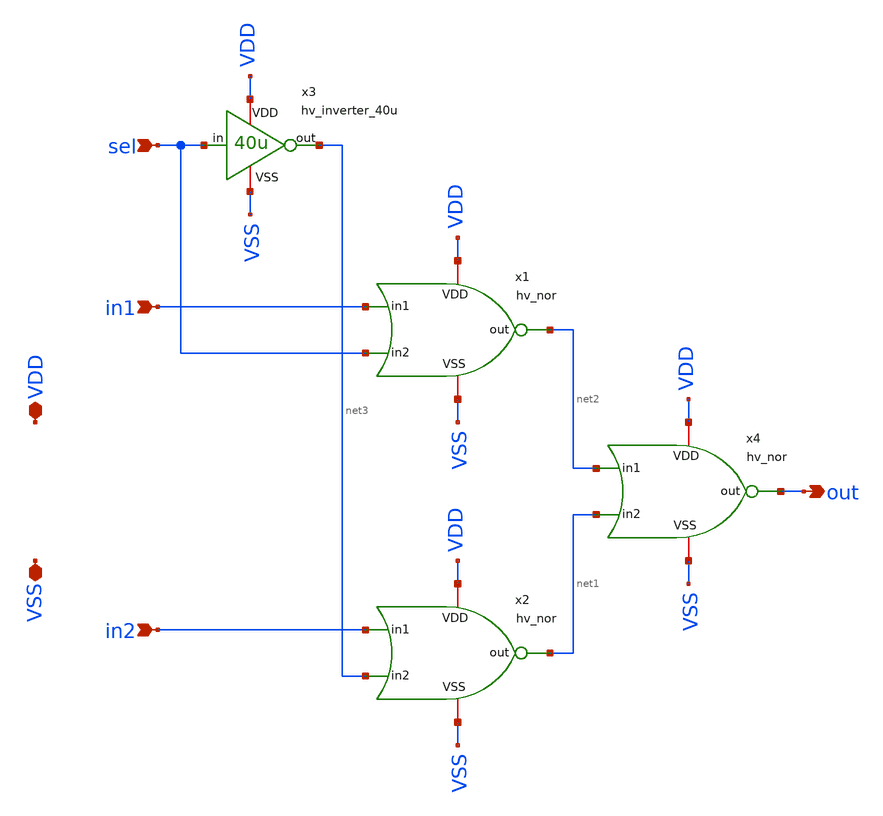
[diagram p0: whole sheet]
** sch_path: macros/heichips26_vcr/macros/switched_capacitor/schematic/xschem/hv_mux.sch
**.subckt hv_mux in1 VDD VSS out in2 sel
*.ipin in1
*.iopin VDD
*.iopin VSS
*.opin out
*.ipin in2
*.ipin sel
x3 VDD sel net3 VSS hv_inverter_40u
x1 VDD in1 net2 sel VSS hv_nor
x2 VDD in2 net1 net3 VSS hv_nor
x4 VDD net2 out net1 VSS hv_nor
**.ends

* expanding   symbol:  hv_inverter_40u.sym # of pins=4
** sym_path: macros/heichips26_vcr/macros/switched_capacitor/schematic/xschem/hv_inverter_40u.sym
** sch_path: macros/heichips26_vcr/macros/switched_capacitor/schematic/xschem/hv_inverter_40u.sch
.subckt hv_inverter_40u VDD in out VSS
*.ipin in
*.iopin VDD
*.iopin VSS
*.opin out
XM2 out in VSS VSS sg13_hv_nmos w={n_w} l={n_l} ng={ng} m=1 mm_ok=1
XM3 out in VDD VDD sg13_hv_pmos w={p_w} l={p_l} ng={ng} m=1 mm_ok=1
**** begin user architecture code


.param w   = 10u
.param ng  = 4
.param n_ng = ng
.param n_w = {3u*n_ng}
.param n_l = 0.45u
.param p_ng = ng
.param p_w = {10u*p_ng}
.param p_l = 0.4u


**** end user architecture code
.ends


* expanding   symbol:  hv_nor.sym # of pins=5
** sym_path: macros/heichips26_vcr/macros/switched_capacitor/schematic/xschem/hv_nor.sym
** sch_path: macros/heichips26_vcr/macros/switched_capacitor/schematic/xschem/hv_nor.sch
.subckt hv_nor VDD in1 out in2 VSS
*.ipin in1
*.iopin VDD
*.iopin VSS
*.opin out
*.ipin in2
**** begin user architecture code


.param w   = 10u
.param ng  = 4
.param n_ng = ng
.param n_w = {3u*n_ng}
.param n_l = 0.45u
.param p_ng = ng
.param p_w = {10u*p_ng}
.param p_l = 0.4u


**** end user architecture code
XM2 out in2 VSS VSS sg13_hv_nmos w={n_w} l={n_l} ng={ng} m=1 mm_ok=1
XM3 net1 in1 VDD VDD sg13_hv_pmos w={p_w} l={p_l} ng={ng} m=1 mm_ok=1
XM1 out in1 VSS VSS sg13_hv_nmos w={n_w} l={n_l} ng={ng} m=1 mm_ok=1
XM4 out in2 net1 VDD sg13_hv_pmos w={p_w} l={p_l} ng={ng} m=1 mm_ok=1
.ends

.end
